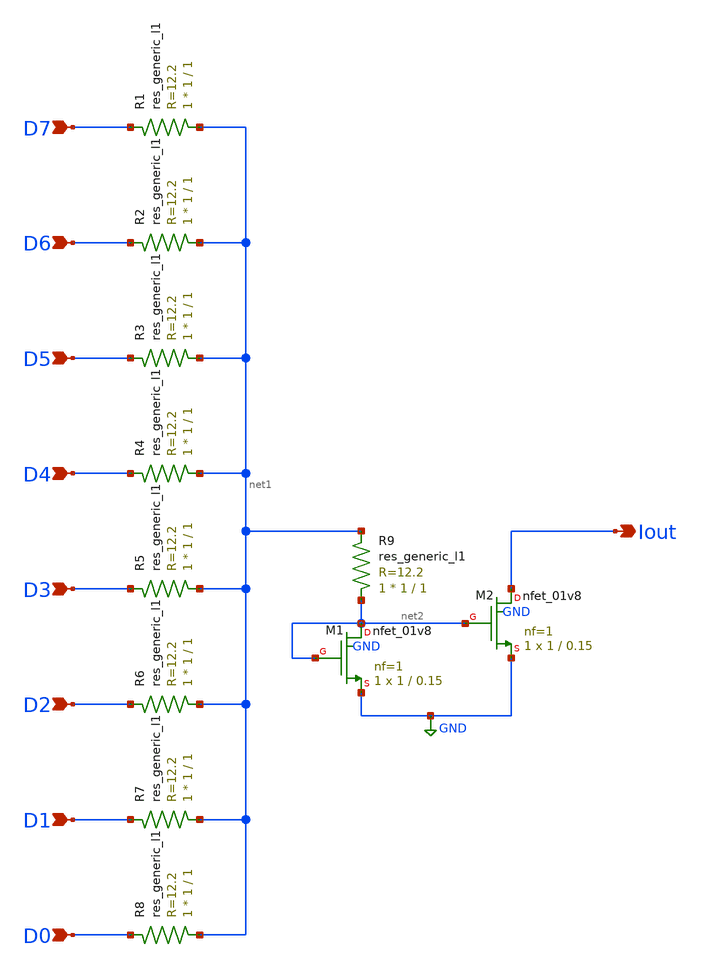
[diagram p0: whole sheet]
** sch_path: analog/schematics/DAC.sch
**.subckt DAC Iout D7 D6 D5 D4 D3 D2 D1 D0
*.opin Iout
*.ipin D7
*.ipin D6
*.ipin D5
*.ipin D4
*.ipin D3
*.ipin D2
*.ipin D1
*.ipin D0
R1 net1 D7 sky130_fd_pr__res_generic_l1 W=1 L=1 m=1
R2 net1 D6 sky130_fd_pr__res_generic_l1 W=1 L=1 m=1
R3 net1 D5 sky130_fd_pr__res_generic_l1 W=1 L=1 m=1
R4 net1 D4 sky130_fd_pr__res_generic_l1 W=1 L=1 m=1
R5 net1 D3 sky130_fd_pr__res_generic_l1 W=1 L=1 m=1
R6 net1 D2 sky130_fd_pr__res_generic_l1 W=1 L=1 m=1
R7 net1 D1 sky130_fd_pr__res_generic_l1 W=1 L=1 m=1
R8 net1 D0 sky130_fd_pr__res_generic_l1 W=1 L=1 m=1
R9 net2 net1 sky130_fd_pr__res_generic_l1 W=1 L=1 m=1
XM1 net2 net2 GND GND sky130_fd_pr__nfet_01v8 L=0.15 W=1 nf=1 ad='int((nf+1)/2) * W/nf * 0.29' as='int((nf+2)/2) * W/nf * 0.29'
+ pd='2*int((nf+1)/2) * (W/nf + 0.29)' ps='2*int((nf+2)/2) * (W/nf + 0.29)' nrd='0.29 / W' nrs='0.29 / W'
+ sa=0 sb=0 sd=0 mult=1 m=1
XM2 Iout net2 GND GND sky130_fd_pr__nfet_01v8 L=0.15 W=1 nf=1 ad='int((nf+1)/2) * W/nf * 0.29' as='int((nf+2)/2) * W/nf * 0.29'
+ pd='2*int((nf+1)/2) * (W/nf + 0.29)' ps='2*int((nf+2)/2) * (W/nf + 0.29)' nrd='0.29 / W' nrs='0.29 / W'
+ sa=0 sb=0 sd=0 mult=1 m=1
**.ends
.GLOBAL GND
.end
